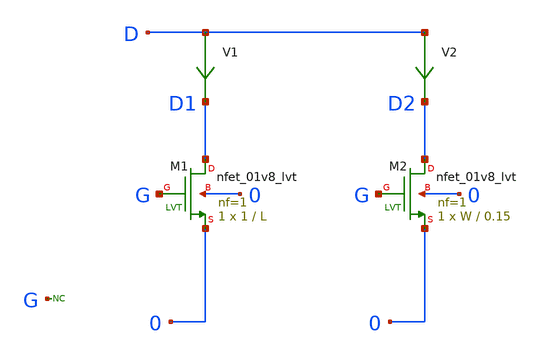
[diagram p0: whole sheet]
** sch_path: sky130A/xschem_libs/sky130_tests/test_nmos_sizes/schematic/test_nmos_sizes.sch
* Copyright 2021 Stefan Frederik Schippers
* Licensed under the Apache License, Version 2.0 (the "License");
* you may not use this file except in compliance with the License.
* You may obtain a copy of the License at
* https://www.apache.org/licenses/LICENSE-2.0
* Unless required by applicable law or agreed to in writing, software
* distributed under the License is distributed on an "AS IS" BASIS,
* WITHOUT WARRANTIES OR CONDITIONS OF ANY KIND, either express or implied.
* See the License for the specific language governing permissions and
* limitations under the License.
**.subckt test_nmos_sizes
XM1 D1 G 0 0 sky130_fd_pr__nfet_01v8_lvt L=L W=1 nf=1 ad='int((1 + 1)/2) * 1 / 1 * 0.29' as='int((1 + 2)/2) * 1 / 1 * 0.29'
+ pd='2*int((1 + 1)/2) * (1 / 1 + 0.29)' ps='2*int((1 + 2)/2) * (1 / 1 + 0.29)' nrd='0.29 / 1 ' nrs='0.29 / 1 '
+ sa=0 sb=0 sd=0 mult=1 m=1
XM2 D2 G 0 0 sky130_fd_pr__nfet_01v8_lvt L=0.15 W=W nf=1 ad='int((1 + 1)/2) * W / 1 * 0.29' as='int((1 + 2)/2) * W / 1 * 0.29'
+ pd='2*int((1 + 1)/2) * (W / 1 + 0.29)' ps='2*int((1 + 2)/2) * (W / 1 + 0.29)' nrd='0.29 / W ' nrs='0.29 / W '
+ sa=0 sb=0 sd=0 mult=1 m=1
V2 D D2 0
.save i(v2)
V1 D D1 0
.save i(v1)
* noconn G
**** begin user architecture code

** opencircuitdesign pdks install
.lib $::SKYWATER_MODELS/sky130.lib.spice tt

**** end user architecture code
**.ends
**** begin user architecture code

* .option SCALE=1e-6
.option method=gear seed=12
.param L=0.15
.param W=0.5
vd d 0 0
vg g 0 0
.control
dc vd 0 2 0.01 vg 0 2 0.2
alterparam L=0.18
alterparam W=1
reset
dc vd 0 2 0.01 vg 0 2 0.2
alterparam L=0.3
alterparam W=2
reset
dc vd 0 2 0.01 vg 0 2 0.2
alterparam L=0.5
alterparam W=3
reset
dc vd 0 2 0.01 vg 0 2 0.2
.endc


**** end user architecture code
.end
